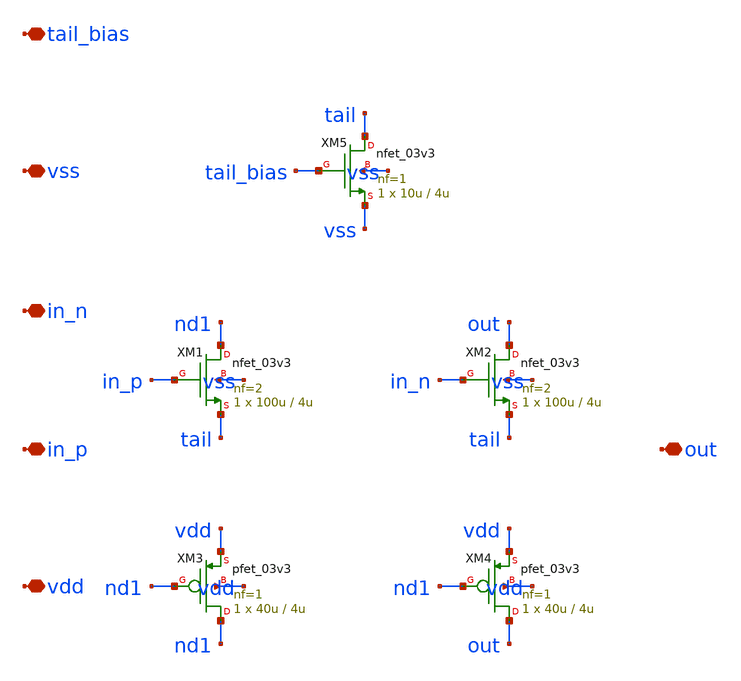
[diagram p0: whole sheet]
** sch_path: design/bandgap_amp.sch
**.subckt bandgap_amp vdd vss in_p in_n out tail_bias
*.iopin vdd
*.iopin vss
*.iopin in_p
*.iopin in_n
*.iopin out
*.iopin tail_bias
XM1 nd1 in_p tail vss nfet_03v3 L=4u W=100u nf=2 ad='int((nf+1)/2) * W/nf * 0.18u' as='int((nf+2)/2) * W/nf * 0.18u'
+ pd='2*int((nf+1)/2) * (W/nf + 0.18u)' ps='2*int((nf+2)/2) * (W/nf + 0.18u)' nrd='0.18u / W' nrs='0.18u / W'
+ sa=0 sb=0 sd=0 m=1
XM2 out in_n tail vss nfet_03v3 L=4u W=100u nf=2 ad='int((nf+1)/2) * W/nf * 0.18u' as='int((nf+2)/2) * W/nf * 0.18u'
+ pd='2*int((nf+1)/2) * (W/nf + 0.18u)' ps='2*int((nf+2)/2) * (W/nf + 0.18u)' nrd='0.18u / W' nrs='0.18u / W'
+ sa=0 sb=0 sd=0 m=1
XM3 nd1 nd1 vdd vdd pfet_03v3 L=4u W=40u nf=1 ad='int((nf+1)/2) * W/nf * 0.18u' as='int((nf+2)/2) * W/nf * 0.18u'
+ pd='2*int((nf+1)/2) * (W/nf + 0.18u)' ps='2*int((nf+2)/2) * (W/nf + 0.18u)' nrd='0.18u / W' nrs='0.18u / W'
+ sa=0 sb=0 sd=0 m=1
XM4 out nd1 vdd vdd pfet_03v3 L=4u W=40u nf=1 ad='int((nf+1)/2) * W/nf * 0.18u' as='int((nf+2)/2) * W/nf * 0.18u'
+ pd='2*int((nf+1)/2) * (W/nf + 0.18u)' ps='2*int((nf+2)/2) * (W/nf + 0.18u)' nrd='0.18u / W' nrs='0.18u / W'
+ sa=0 sb=0 sd=0 m=1
XM5 tail tail_bias vss vss nfet_03v3 L=4u W=10u nf=1 ad='int((nf+1)/2) * W/nf * 0.18u' as='int((nf+2)/2) * W/nf * 0.18u'
+ pd='2*int((nf+1)/2) * (W/nf + 0.18u)' ps='2*int((nf+2)/2) * (W/nf + 0.18u)' nrd='0.18u / W' nrs='0.18u / W'
+ sa=0 sb=0 sd=0 m=1
**.ends
.end
